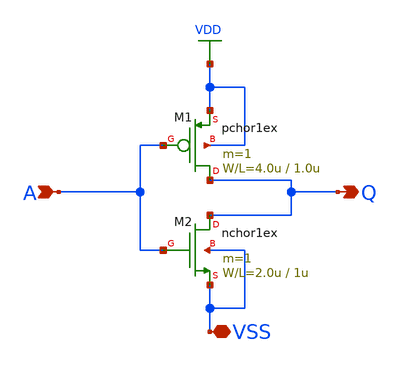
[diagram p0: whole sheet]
** sch_path: member_project/wwlapaki310/inverter.sch
**.subckt inverter A Q VSS
*.ipin A
*.opin Q
*.iopin VSS
M1 Q A VDD VDD pchor1ex L=1.0u W=4.0u m=1
M2 Q A VSS VSS nchor1ex L=1u W=2.0u m=1
**.ends
.GLOBAL VDD
.end
